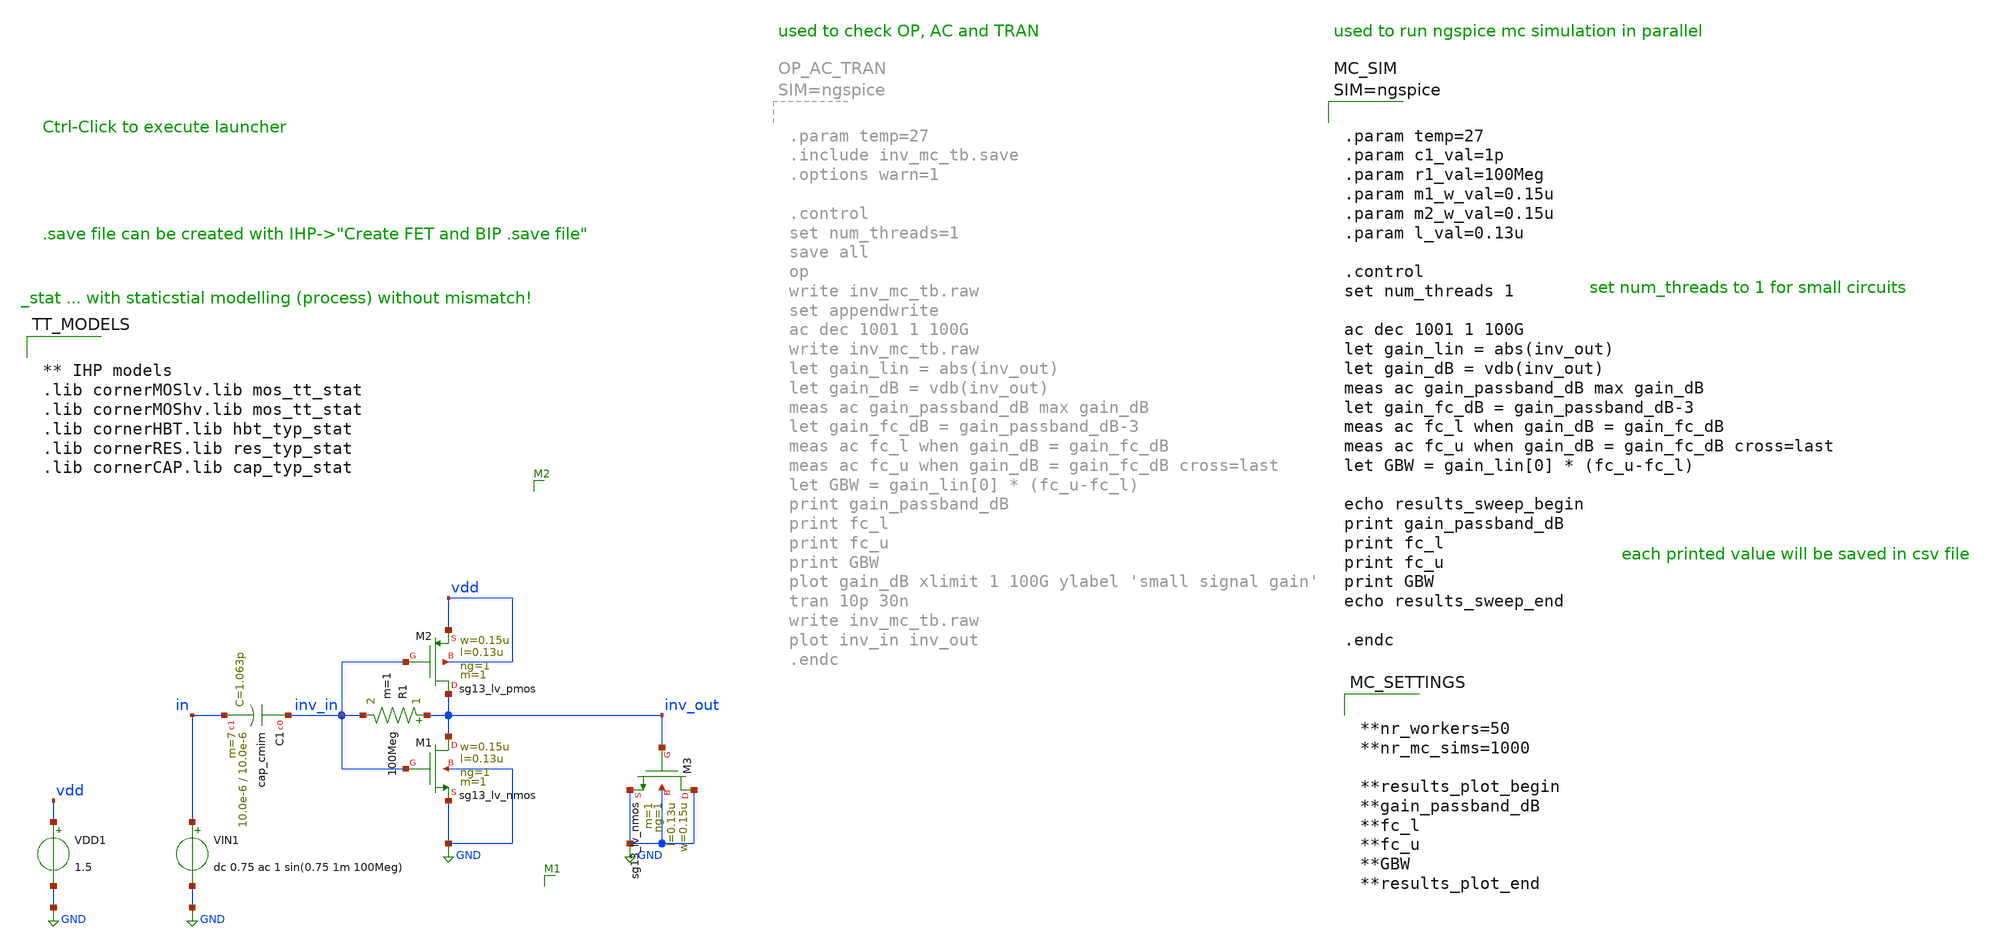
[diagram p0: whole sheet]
** sch_path: ihp-sg13g2/libs.tech/xschem/sg13g2_tests/inv_mc_tb.sch
**.subckt inv_mc_tb
VDD1 vdd GND 1.5
XM1 inv_out inv_in GND GND sg13_lv_nmos w=0.15u l=0.13u ng=1 m=1 mm_ok=1
XM2 inv_out inv_in vdd vdd sg13_lv_pmos w=0.15u l=0.13u ng=1 m=1 mm_ok=1
XM3 GND inv_out GND GND sg13_lv_nmos w=0.15u l=0.13u ng=1 m=1 mm_ok=1
VIN1 in GND dc 0.75 ac 1 sin(0.75 1m 100Meg)
R1 inv_out inv_in 100Meg m=1
XC1 inv_in in cap_cmim w=10.0e-6 l=10.0e-6 m=7 mm_ok=1
**** begin user architecture code


** IHP models
.lib cornerMOSlv.lib mos_tt_stat
.lib cornerMOShv.lib mos_tt_stat
.lib cornerHBT.lib hbt_typ_stat
.lib cornerRES.lib res_typ_stat
.lib cornerCAP.lib cap_typ_stat





.param temp=27
.param c1_val=1p
.param r1_val=100Meg
.param m1_w_val=0.15u
.param m2_w_val=0.15u
.param l_val=0.13u

.control
set num_threads 1

ac dec 1001 1 100G
let gain_lin = abs(inv_out)
let gain_dB = vdb(inv_out)
meas ac gain_passband_dB max gain_dB
let gain_fc_dB = gain_passband_dB-3
meas ac fc_l when gain_dB = gain_fc_dB
meas ac fc_u when gain_dB = gain_fc_dB cross=last
let GBW = gain_lin[0] * (fc_u-fc_l)

echo results_sweep_begin
print gain_passband_dB
print fc_l
print fc_u
print GBW
echo results_sweep_end

.endc





**nr_workers=50
**nr_mc_sims=1000

**results_plot_begin
**gain_passband_dB
**fc_l
**fc_u
**GBW
**results_plot_end


**** end user architecture code
**.ends
.GLOBAL GND
.end
